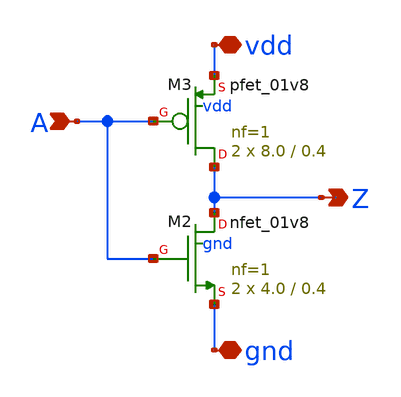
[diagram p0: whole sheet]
** sch_path: sram_2_64_scn4m/pinv_12.sch
**.subckt pinv_12 A Z vdd gnd
*.ipin A
*.opin Z
*.iopin vdd
*.iopin gnd
XM2 Z A gnd gnd sky130_fd_pr__nfet_01v8 L=0.4 W=4.0 nf=1 ad='int((nf+1)/2) * W/nf * 0.29' as='int((nf+2)/2) * W/nf * 0.29'
+ pd='2*int((nf+1)/2) * (W/nf + 0.29)' ps='2*int((nf+2)/2) * (W/nf + 0.29)' nrd='0.29 / W' nrs='0.29 / W'
+ sa=0 sb=0 sd=0 mult=2 m=2
XM3 Z A vdd vdd sky130_fd_pr__pfet_01v8 L=0.4 W=8.0 nf=1 ad='int((nf+1)/2) * W/nf * 0.29' as='int((nf+2)/2) * W/nf * 0.29'
+ pd='2*int((nf+1)/2) * (W/nf + 0.29)' ps='2*int((nf+2)/2) * (W/nf + 0.29)' nrd='0.29 / W' nrs='0.29 / W'
+ sa=0 sb=0 sd=0 mult=2 m=2
**.ends
.end
